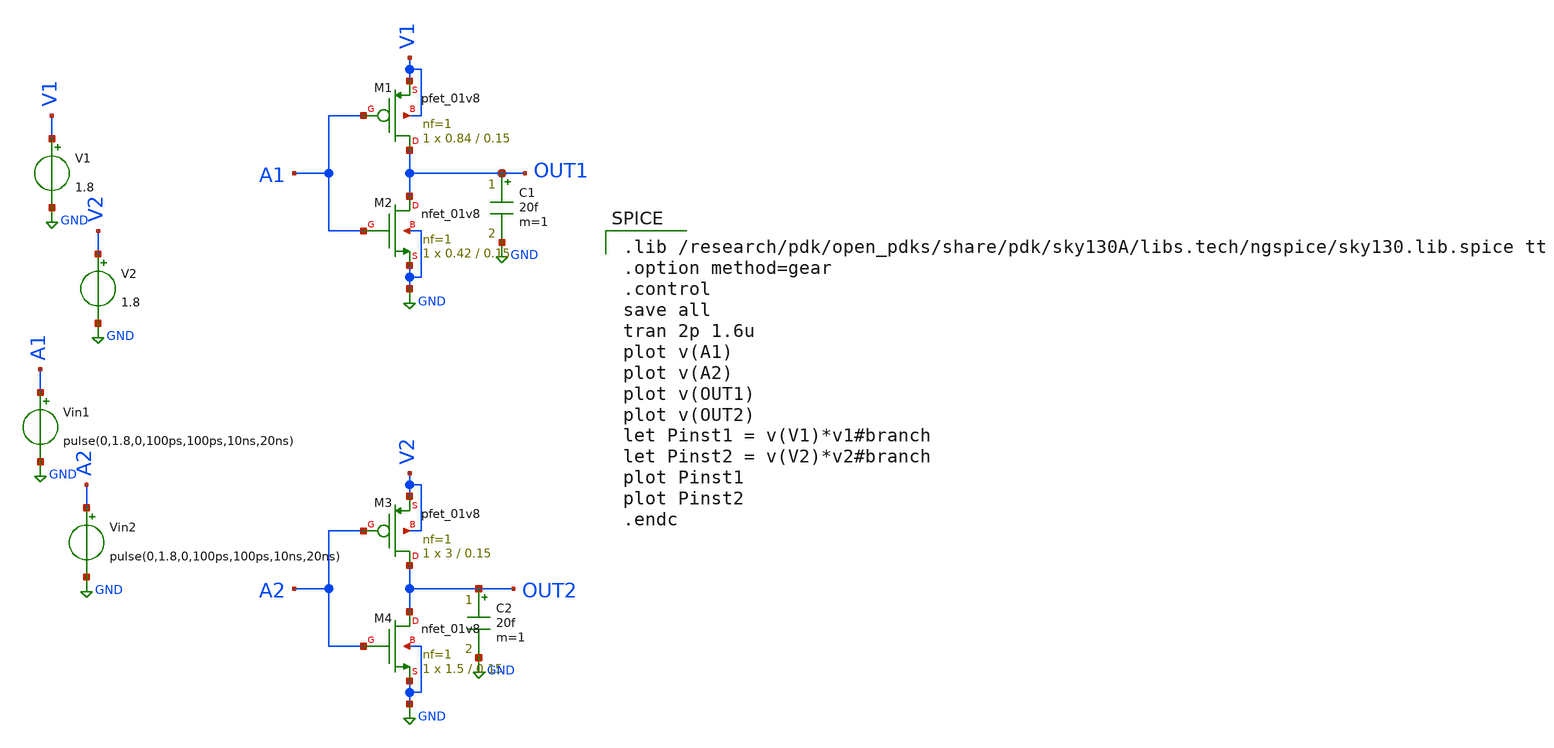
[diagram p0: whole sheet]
** sch_path: skywater_stuff/untitled-19.sch
**.subckt untitled-19
XM1 OUT1 A1 V1 V1 sky130_fd_pr__pfet_01v8 L=0.15 W=0.84 nf=1 ad='int((nf+1)/2) * W/nf * 0.29' as='int((nf+2)/2) * W/nf * 0.29'
+ pd='2*int((nf+1)/2) * (W/nf + 0.29)' ps='2*int((nf+2)/2) * (W/nf + 0.29)' nrd='0.29 / W' nrs='0.29 / W'
+ sa=0 sb=0 sd=0 mult=1 m=1
XM2 OUT1 A1 GND GND sky130_fd_pr__nfet_01v8 L=0.15 W=0.42 nf=1 ad='int((nf+1)/2) * W/nf * 0.29' as='int((nf+2)/2) * W/nf * 0.29'
+ pd='2*int((nf+1)/2) * (W/nf + 0.29)' ps='2*int((nf+2)/2) * (W/nf + 0.29)' nrd='0.29 / W' nrs='0.29 / W'
+ sa=0 sb=0 sd=0 mult=1 m=1
XM3 OUT2 A2 V2 V2 sky130_fd_pr__pfet_01v8 L=0.15 W=3 nf=1 ad='int((nf+1)/2) * W/nf * 0.29' as='int((nf+2)/2) * W/nf * 0.29'
+ pd='2*int((nf+1)/2) * (W/nf + 0.29)' ps='2*int((nf+2)/2) * (W/nf + 0.29)' nrd='0.29 / W' nrs='0.29 / W'
+ sa=0 sb=0 sd=0 mult=1 m=1
XM4 OUT2 A2 GND GND sky130_fd_pr__nfet_01v8 L=0.15 W=1.5 nf=1 ad='int((nf+1)/2) * W/nf * 0.29' as='int((nf+2)/2) * W/nf * 0.29'
+ pd='2*int((nf+1)/2) * (W/nf + 0.29)' ps='2*int((nf+2)/2) * (W/nf + 0.29)' nrd='0.29 / W' nrs='0.29 / W'
+ sa=0 sb=0 sd=0 mult=1 m=1
V1 V1 GND 1.8
V2 V2 GND 1.8
Vin1 A1 GND pulse(0,1.8,0,100ps,100ps,10ns,20ns)
Vin2 A2 GND pulse(0,1.8,0,100ps,100ps,10ns,20ns)
C1 OUT1 GND 20f m=1
C2 OUT2 GND 20f m=1
**** begin user architecture code

.lib /research/pdk/open_pdks/share/pdk/sky130A/libs.tech/ngspice/sky130.lib.spice tt
.option method=gear
.control
save all
tran 2p 1.6u
plot v(A1)
plot v(A2)
plot v(OUT1)
plot v(OUT2)
let Pinst1 = v(V1)*v1#branch
let Pinst2 = v(V2)*v2#branch
plot Pinst1
plot Pinst2
.endc


**** end user architecture code
**.ends
.GLOBAL GND
.end
